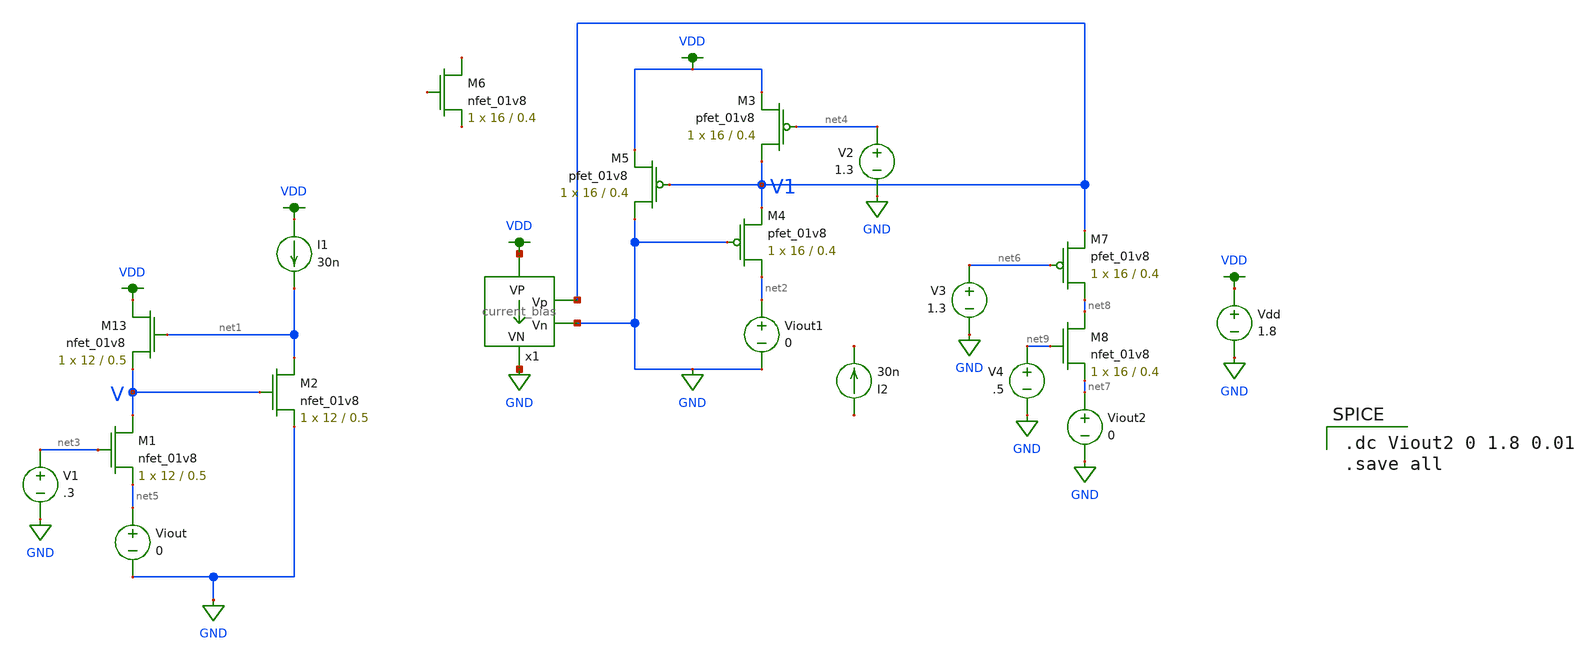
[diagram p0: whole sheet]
** sch_path: Final DAC files/schematics/MOS_cascode_circuit.sch
**.subckt MOS_cascode_circuit
XM13 VDD net1 V GND sky130_fd_pr__nfet_01v8 L=0.5 W=12 nf=1 ad='int((nf+1)/2) * W/nf * 0.29' as='int((nf+2)/2) * W/nf * 0.29'
+ pd='2*int((nf+1)/2) * (W/nf + 0.29)' ps='2*int((nf+2)/2) * (W/nf + 0.29)' nrd='0.29 / W' nrs='0.29 / W'
+ sa=0 sb=0 sd=0 mult=1 m=1
XM1 V net3 net5 GND sky130_fd_pr__nfet_01v8 L=0.5 W=12 nf=1 ad='int((nf+1)/2) * W/nf * 0.29' as='int((nf+2)/2) * W/nf * 0.29'
+ pd='2*int((nf+1)/2) * (W/nf + 0.29)' ps='2*int((nf+2)/2) * (W/nf + 0.29)' nrd='0.29 / W' nrs='0.29 / W'
+ sa=0 sb=0 sd=0 mult=1 m=1
XM2 net1 V GND GND sky130_fd_pr__nfet_01v8 L=0.5 W=12 nf=1 ad='int((nf+1)/2) * W/nf * 0.29' as='int((nf+2)/2) * W/nf * 0.29'
+ pd='2*int((nf+1)/2) * (W/nf + 0.29)' ps='2*int((nf+2)/2) * (W/nf + 0.29)' nrd='0.29 / W' nrs='0.29 / W'
+ sa=0 sb=0 sd=0 mult=1 m=1
Vdd VDD GND 1.8
I1 VDD net1 30n
V1 net3 GND .3
XM3 V1 net4 VDD VDD sky130_fd_pr__pfet_01v8 L=0.4 W=16 nf=1 ad='int((nf+1)/2) * W/nf * 0.29' as='int((nf+2)/2) * W/nf * 0.29'
+ pd='2*int((nf+1)/2) * (W/nf + 0.29)' ps='2*int((nf+2)/2) * (W/nf + 0.29)' nrd='0.29 / W' nrs='0.29 / W'
+ sa=0 sb=0 sd=0 mult=1 m=1
XM4 net2 GND V1 VDD sky130_fd_pr__pfet_01v8 L=0.4 W=16 nf=1 ad='int((nf+1)/2) * W/nf * 0.29' as='int((nf+2)/2) * W/nf * 0.29'
+ pd='2*int((nf+1)/2) * (W/nf + 0.29)' ps='2*int((nf+2)/2) * (W/nf + 0.29)' nrd='0.29 / W' nrs='0.29 / W'
+ sa=0 sb=0 sd=0 mult=1 m=1
XM5 GND V1 VDD VDD sky130_fd_pr__pfet_01v8 L=0.4 W=16 nf=1 ad='int((nf+1)/2) * W/nf * 0.29' as='int((nf+2)/2) * W/nf * 0.29'
+ pd='2*int((nf+1)/2) * (W/nf + 0.29)' ps='2*int((nf+2)/2) * (W/nf + 0.29)' nrd='0.29 / W' nrs='0.29 / W'
+ sa=0 sb=0 sd=0 mult=1 m=1
I2 net10 net11 30n
XM6 net12 net13 net14 GND sky130_fd_pr__nfet_01v8 L=0.4 W=16 nf=1 ad='int((nf+1)/2) * W/nf * 0.29' as='int((nf+2)/2) * W/nf * 0.29'
+ pd='2*int((nf+1)/2) * (W/nf + 0.29)' ps='2*int((nf+2)/2) * (W/nf + 0.29)' nrd='0.29 / W' nrs='0.29 / W'
+ sa=0 sb=0 sd=0 mult=1 m=1
V2 net4 GND 1.3
Viout net5 GND 0
x1 VDD GND GND V1 current_bias
Viout1 net2 GND 0
XM7 net8 net6 V1 VDD sky130_fd_pr__pfet_01v8 L=0.4 W=16 nf=1 ad='int((nf+1)/2) * W/nf * 0.29' as='int((nf+2)/2) * W/nf * 0.29'
+ pd='2*int((nf+1)/2) * (W/nf + 0.29)' ps='2*int((nf+2)/2) * (W/nf + 0.29)' nrd='0.29 / W' nrs='0.29 / W'
+ sa=0 sb=0 sd=0 mult=1 m=1
Viout2 net7 GND 0
V3 net6 GND 1.3
XM8 net8 net9 net7 GND sky130_fd_pr__nfet_01v8 L=0.4 W=16 nf=1 ad='int((nf+1)/2) * W/nf * 0.29' as='int((nf+2)/2) * W/nf * 0.29'
+ pd='2*int((nf+1)/2) * (W/nf + 0.29)' ps='2*int((nf+2)/2) * (W/nf + 0.29)' nrd='0.29 / W' nrs='0.29 / W'
+ sa=0 sb=0 sd=0 mult=1 m=1
V4 net9 GND .5
**** begin user architecture code

.option wnflag=1
.param MC_SWITCH=1.0
.lib ~/skywater/skywater-pdk/libraries/sky130_fd_pr_ngspice/latest/models/sky130.lib.spice tt


.dc Viout2 0 1.8 0.01
.save all

**** end user architecture code
**.ends

* expanding   symbol:  /home/madvlsi/dev/git/7-bit-D-A-converter-MP4-MADVLSI/Final DAC files/current
*+ bias/current_bias.sym # of pins=4
** sym_path: Final DAC files/current bias/current_bias.sym
** sch_path: Final DAC files/current bias/current_bias.sch
.subckt current_bias VP Vn VN Vp
*.iopin VP
*.iopin VN
*.opin Vn
*.opin Vp
XM4 net1 net1 net3 GND sky130_fd_pr__nfet_01v8 L=0.5 W=12 nf=1 ad='int((nf+1)/2) * W/nf * 0.29' as='int((nf+2)/2) * W/nf * 0.29'
+ pd='2*int((nf+1)/2) * (W/nf + 0.29)' ps='2*int((nf+2)/2) * (W/nf + 0.29)' nrd='0.29 / W' nrs='0.29 / W'
+ sa=0 sb=0 sd=0 mult=8 m=8
XM5 net2 net1 VN GND sky130_fd_pr__nfet_01v8 L=0.5 W=12 nf=1 ad='int((nf+1)/2) * W/nf * 0.29' as='int((nf+2)/2) * W/nf * 0.29'
+ pd='2*int((nf+1)/2) * (W/nf + 0.29)' ps='2*int((nf+2)/2) * (W/nf + 0.29)' nrd='0.29 / W' nrs='0.29 / W'
+ sa=0 sb=0 sd=0 mult=1 m=1
XM6 Vp Vn VN GND sky130_fd_pr__nfet_01v8 L=0.5 W=12 nf=1 ad='int((nf+1)/2) * W/nf * 0.29' as='int((nf+2)/2) * W/nf * 0.29'
+ pd='2*int((nf+1)/2) * (W/nf + 0.29)' ps='2*int((nf+2)/2) * (W/nf + 0.29)' nrd='0.29 / W' nrs='0.29 / W'
+ sa=0 sb=0 sd=0 mult=1 m=1
XM7 Vn Vn VN GND sky130_fd_pr__nfet_01v8 L=0.5 W=12 nf=1 ad='int((nf+1)/2) * W/nf * 0.29' as='int((nf+2)/2) * W/nf * 0.29'
+ pd='2*int((nf+1)/2) * (W/nf + 0.29)' ps='2*int((nf+2)/2) * (W/nf + 0.29)' nrd='0.29 / W' nrs='0.29 / W'
+ sa=0 sb=0 sd=0 mult=1 m=1
R1 net3 VN 100k m=1
XM8 Vp net2 VP VDD sky130_fd_pr__pfet_01v8 L=0.5 W=12 nf=1 ad='int((nf+1)/2) * W/nf * 0.29' as='int((nf+2)/2) * W/nf * 0.29'
+ pd='2*int((nf+1)/2) * (W/nf + 0.29)' ps='2*int((nf+2)/2) * (W/nf + 0.29)' nrd='0.29 / W' nrs='0.29 / W'
+ sa=0 sb=0 sd=0 mult=1 m=1
XM9 Vn Vp VP VDD sky130_fd_pr__pfet_01v8 L=0.5 W=12 nf=1 ad='int((nf+1)/2) * W/nf * 0.29' as='int((nf+2)/2) * W/nf * 0.29'
+ pd='2*int((nf+1)/2) * (W/nf + 0.29)' ps='2*int((nf+2)/2) * (W/nf + 0.29)' nrd='0.29 / W' nrs='0.29 / W'
+ sa=0 sb=0 sd=0 mult=1 m=1
XM10 net2 net2 VP VDD sky130_fd_pr__pfet_01v8 L=0.5 W=12 nf=1 ad='int((nf+1)/2) * W/nf * 0.29' as='int((nf+2)/2) * W/nf * 0.29'
+ pd='2*int((nf+1)/2) * (W/nf + 0.29)' ps='2*int((nf+2)/2) * (W/nf + 0.29)' nrd='0.29 / W' nrs='0.29 / W'
+ sa=0 sb=0 sd=0 mult=1 m=1
XM11 net1 Vp VP VDD sky130_fd_pr__pfet_01v8 L=0.5 W=12 nf=1 ad='int((nf+1)/2) * W/nf * 0.29' as='int((nf+2)/2) * W/nf * 0.29'
+ pd='2*int((nf+1)/2) * (W/nf + 0.29)' ps='2*int((nf+2)/2) * (W/nf + 0.29)' nrd='0.29 / W' nrs='0.29 / W'
+ sa=0 sb=0 sd=0 mult=1 m=1
.ends

.GLOBAL GND
.GLOBAL VDD
.end
